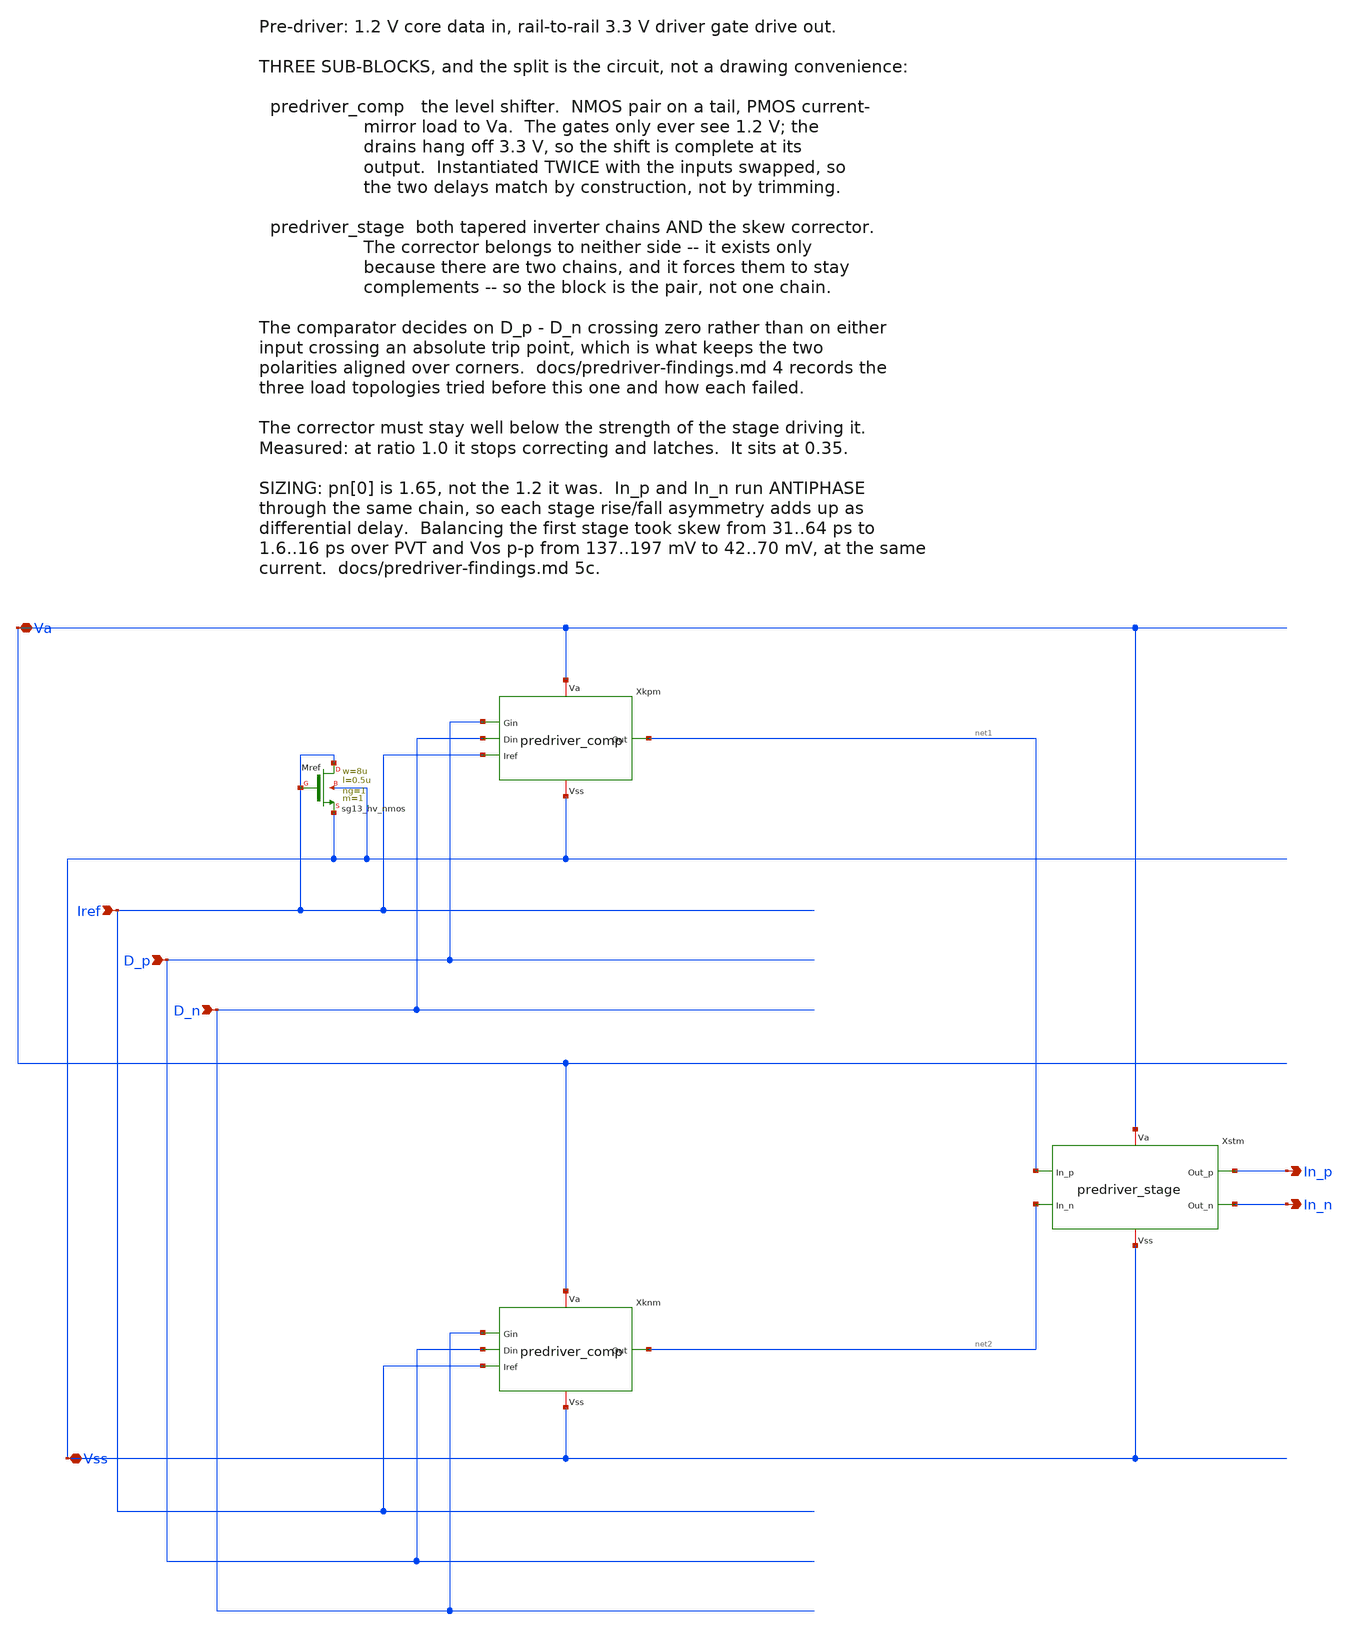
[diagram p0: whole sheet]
** sch_path: macros/lvds_tx/schematic/xschem/predriver.sch
**.subckt predriver Va Vss Iref D_p D_n In_p In_n
*.iopin Va
*.iopin Vss
*.ipin Iref
*.ipin D_p
*.ipin D_n
*.opin In_p
*.opin In_n
Xkpm D_p D_n Iref net1 Va Vss predriver_comp
XMref Iref Iref Vss Vss sg13_hv_nmos w=8u l=0.5u ng=1 m=1 mm_ok=1
Xknm D_n D_p Iref net2 Va Vss predriver_comp
Xstm net1 net2 In_p In_n Va Vss predriver_stage
**.ends

* expanding   symbol:  predriver_comp.sym # of pins=6
** sym_path: macros/lvds_tx/schematic/xschem/predriver_comp.sym
** sch_path: macros/lvds_tx/schematic/xschem/predriver_comp.sch
.subckt predriver_comp Gin Din Iref Out Va Vss
*.iopin Va
*.iopin Vss
*.opin Out
*.ipin Din
*.ipin Gin
*.ipin Iref
XMld net1 net1 Va Va sg13_hv_pmos w=12u l=0.4u ng=4 m=1 mm_ok=1
XMlo Out net1 Va Va sg13_hv_pmos w=12u l=0.4u ng=4 m=1 mm_ok=1
XMid net1 Din net2 Vss sg13_hv_nmos w=24u l=0.45u ng=6 m=1 mm_ok=1
XMio Out Gin net2 Vss sg13_hv_nmos w=24u l=0.45u ng=6 m=1 mm_ok=1
XMt net2 Iref Vss Vss sg13_hv_nmos w=17.52u l=0.45u ng=6 m=2 mm_ok=1
.ends


* expanding   symbol:  predriver_stage.sym # of pins=6
** sym_path: macros/lvds_tx/schematic/xschem/predriver_stage.sym
** sch_path: macros/lvds_tx/schematic/xschem/predriver_stage.sch
.subckt predriver_stage In_p In_n Out_p Out_n Va Vss
*.ipin In_p
*.opin Out_p
*.ipin In_n
*.opin Out_n
*.iopin Va
*.iopin Vss
XMpp0 net1 In_p Va Va sg13_hv_pmos w=2.64u l=0.4u ng=1 m=1 mm_ok=1
XMnp0 net1 In_p Vss Vss sg13_hv_nmos w=1.6u l=0.45u ng=1 m=1 mm_ok=1
XMpp1 net2 net1 Va Va sg13_hv_pmos w=12.52u l=0.4u ng=4 m=1 mm_ok=1
XMnp1 net2 net1 Vss Vss sg13_hv_nmos w=5u l=0.45u ng=4 m=1 mm_ok=1
XMpp2 Out_p net2 Va Va sg13_hv_pmos w=40u l=0.4u ng=10 m=1 mm_ok=1
XMnp2 Out_p net2 Vss Vss sg13_hv_nmos w=16u l=0.45u ng=10 m=1 mm_ok=1
XMpn0 net3 In_n Va Va sg13_hv_pmos w=2.64u l=0.4u ng=1 m=1 mm_ok=1
XMnn0 net3 In_n Vss Vss sg13_hv_nmos w=1.6u l=0.45u ng=1 m=1 mm_ok=1
XMpn1 net4 net3 Va Va sg13_hv_pmos w=12.52u l=0.4u ng=4 m=1 mm_ok=1
XMnn1 net4 net3 Vss Vss sg13_hv_nmos w=5u l=0.45u ng=4 m=1 mm_ok=1
XMpn2 Out_n net4 Va Va sg13_hv_pmos w=40u l=0.4u ng=10 m=1 mm_ok=1
XMnn2 Out_n net4 Vss Vss sg13_hv_nmos w=16u l=0.45u ng=10 m=1 mm_ok=1
XMpxp net4 net2 Va Va sg13_hv_pmos w=4.38u l=0.4u ng=1 m=1 mm_ok=1
XMnxp net4 net2 Vss Vss sg13_hv_nmos w=1.75u l=0.45u ng=1 m=1 mm_ok=1
XMpxn net2 net4 Va Va sg13_hv_pmos w=4.38u l=0.4u ng=1 m=1 mm_ok=1
XMnxn net2 net4 Vss Vss sg13_hv_nmos w=1.75u l=0.45u ng=1 m=1 mm_ok=1
.ends

.end
